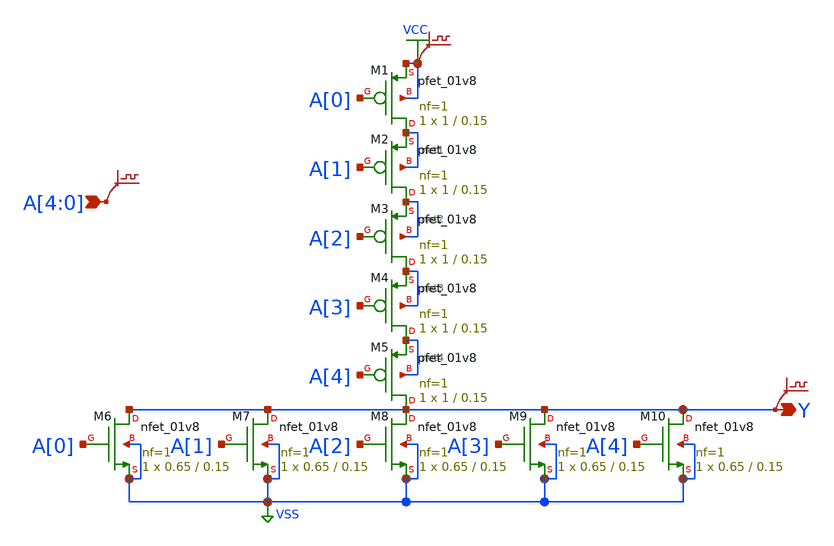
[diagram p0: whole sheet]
** sch_path: elements/nor5.sch
**.subckt nor5 A[4],A[3],A[2],A[1],A[0] Y
*.ipin A[4],A[3],A[2],A[1],A[0]
*.opin Y
XM1 net1 A[0] VCC VCC sky130_fd_pr__pfet_01v8 L=0.15 W=1 nf=1 ad='int((nf+1)/2) * W/nf * 0.29' as='int((nf+2)/2) * W/nf * 0.29'
+ pd='2*int((nf+1)/2) * (W/nf + 0.29)' ps='2*int((nf+2)/2) * (W/nf + 0.29)' nrd='0.29 / W' nrs='0.29 / W'
+ sa=0 sb=0 sd=0 mult=1 m=1
XM2 net2 A[1] net1 net1 sky130_fd_pr__pfet_01v8 L=0.15 W=1 nf=1 ad='int((nf+1)/2) * W/nf * 0.29' as='int((nf+2)/2) * W/nf * 0.29'
+ pd='2*int((nf+1)/2) * (W/nf + 0.29)' ps='2*int((nf+2)/2) * (W/nf + 0.29)' nrd='0.29 / W' nrs='0.29 / W'
+ sa=0 sb=0 sd=0 mult=1 m=1
.save v(a[4])
.save v(a[3])
.save v(a[2])
.save v(a[1])
.save v(a[0])
.save v(y)
.save v(vcc)
XM3 net3 A[2] net2 net2 sky130_fd_pr__pfet_01v8 L=0.15 W=1 nf=1 ad='int((nf+1)/2) * W/nf * 0.29' as='int((nf+2)/2) * W/nf * 0.29'
+ pd='2*int((nf+1)/2) * (W/nf + 0.29)' ps='2*int((nf+2)/2) * (W/nf + 0.29)' nrd='0.29 / W' nrs='0.29 / W'
+ sa=0 sb=0 sd=0 mult=1 m=1
XM4 net4 A[3] net3 net3 sky130_fd_pr__pfet_01v8 L=0.15 W=1 nf=1 ad='int((nf+1)/2) * W/nf * 0.29' as='int((nf+2)/2) * W/nf * 0.29'
+ pd='2*int((nf+1)/2) * (W/nf + 0.29)' ps='2*int((nf+2)/2) * (W/nf + 0.29)' nrd='0.29 / W' nrs='0.29 / W'
+ sa=0 sb=0 sd=0 mult=1 m=1
XM5 Y A[4] net4 net4 sky130_fd_pr__pfet_01v8 L=0.15 W=1 nf=1 ad='int((nf+1)/2) * W/nf * 0.29' as='int((nf+2)/2) * W/nf * 0.29'
+ pd='2*int((nf+1)/2) * (W/nf + 0.29)' ps='2*int((nf+2)/2) * (W/nf + 0.29)' nrd='0.29 / W' nrs='0.29 / W'
+ sa=0 sb=0 sd=0 mult=1 m=1
XM6 Y A[0] VSS VSS sky130_fd_pr__nfet_01v8 L=0.15 W=0.65 nf=1 ad='int((1 + 1)/2) * 0.65 / 1 * 0.29' as='int((1 + 2)/2) * 0.65 / 1 * 0.29'
+ pd='2*int((1 + 1)/2) * (0.65 / 1 + 0.29)' ps='2*int((1 + 2)/2) * (0.65 / 1 + 0.29)' nrd='0.29 / 0.65 '
+ nrs='0.29 / 0.65 ' sa=0 sb=0 sd=0 mult=1 m=1
XM7 Y A[1] VSS VSS sky130_fd_pr__nfet_01v8 L=0.15 W=0.65 nf=1 ad='int((1 + 1)/2) * 0.65 / 1 * 0.29' as='int((1 + 2)/2) * 0.65 / 1 * 0.29'
+ pd='2*int((1 + 1)/2) * (0.65 / 1 + 0.29)' ps='2*int((1 + 2)/2) * (0.65 / 1 + 0.29)' nrd='0.29 / 0.65 '
+ nrs='0.29 / 0.65 ' sa=0 sb=0 sd=0 mult=1 m=1
XM8 Y A[2] VSS VSS sky130_fd_pr__nfet_01v8 L=0.15 W=0.65 nf=1 ad='int((1 + 1)/2) * 0.65 / 1 * 0.29' as='int((1 + 2)/2) * 0.65 / 1 * 0.29'
+ pd='2*int((1 + 1)/2) * (0.65 / 1 + 0.29)' ps='2*int((1 + 2)/2) * (0.65 / 1 + 0.29)' nrd='0.29 / 0.65 '
+ nrs='0.29 / 0.65 ' sa=0 sb=0 sd=0 mult=1 m=1
XM9 Y A[3] VSS VSS sky130_fd_pr__nfet_01v8 L=0.15 W=0.65 nf=1 ad='int((1 + 1)/2) * 0.65 / 1 * 0.29' as='int((1 + 2)/2) * 0.65 / 1 * 0.29'
+ pd='2*int((1 + 1)/2) * (0.65 / 1 + 0.29)' ps='2*int((1 + 2)/2) * (0.65 / 1 + 0.29)' nrd='0.29 / 0.65 '
+ nrs='0.29 / 0.65 ' sa=0 sb=0 sd=0 mult=1 m=1
XM10 Y A[4] VSS VSS sky130_fd_pr__nfet_01v8 L=0.15 W=0.65 nf=1 ad='int((1 + 1)/2) * 0.65 / 1 * 0.29'
+ as='int((1 + 2)/2) * 0.65 / 1 * 0.29' pd='2*int((1 + 1)/2) * (0.65 / 1 + 0.29)' ps='2*int((1 + 2)/2) * (0.65 / 1 + 0.29)'
+ nrd='0.29 / 0.65 ' nrs='0.29 / 0.65 ' sa=0 sb=0 sd=0 mult=1 m=1
**.ends
.GLOBAL VCC
.GLOBAL VSS
.end
